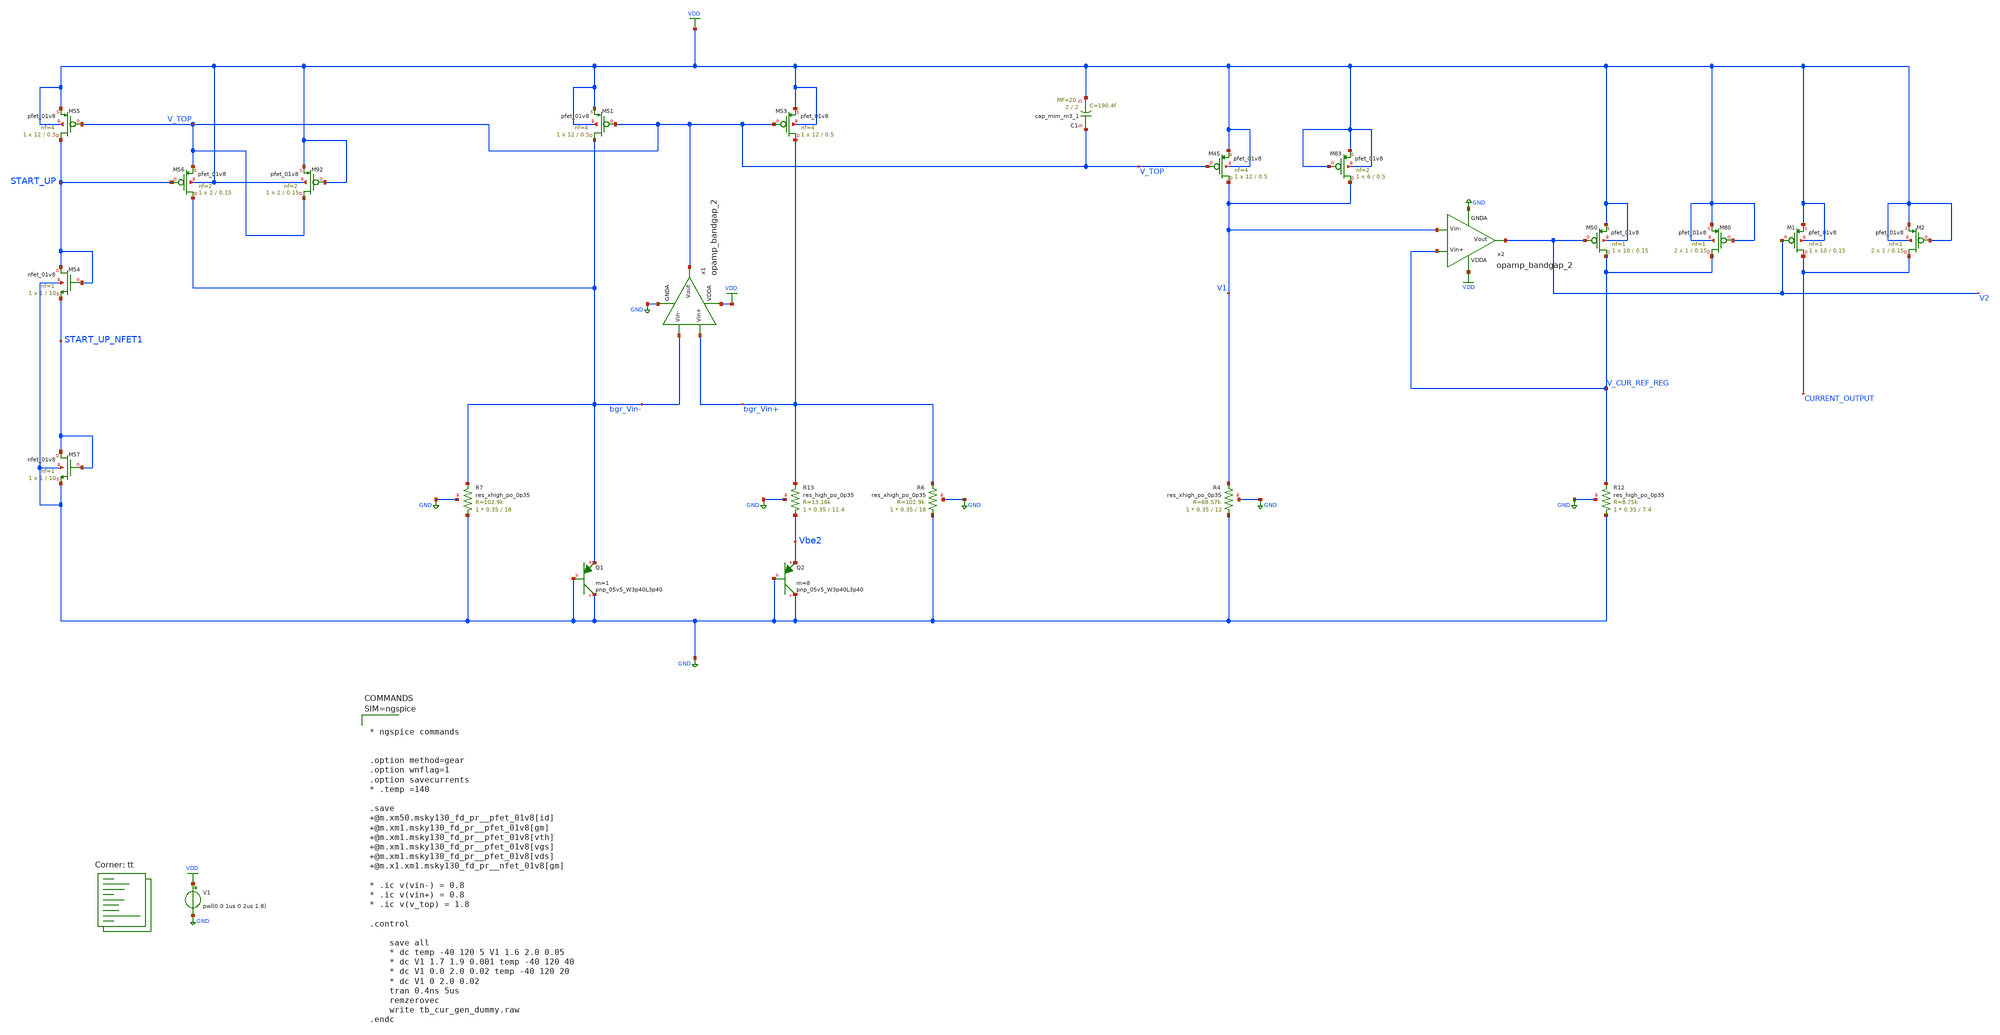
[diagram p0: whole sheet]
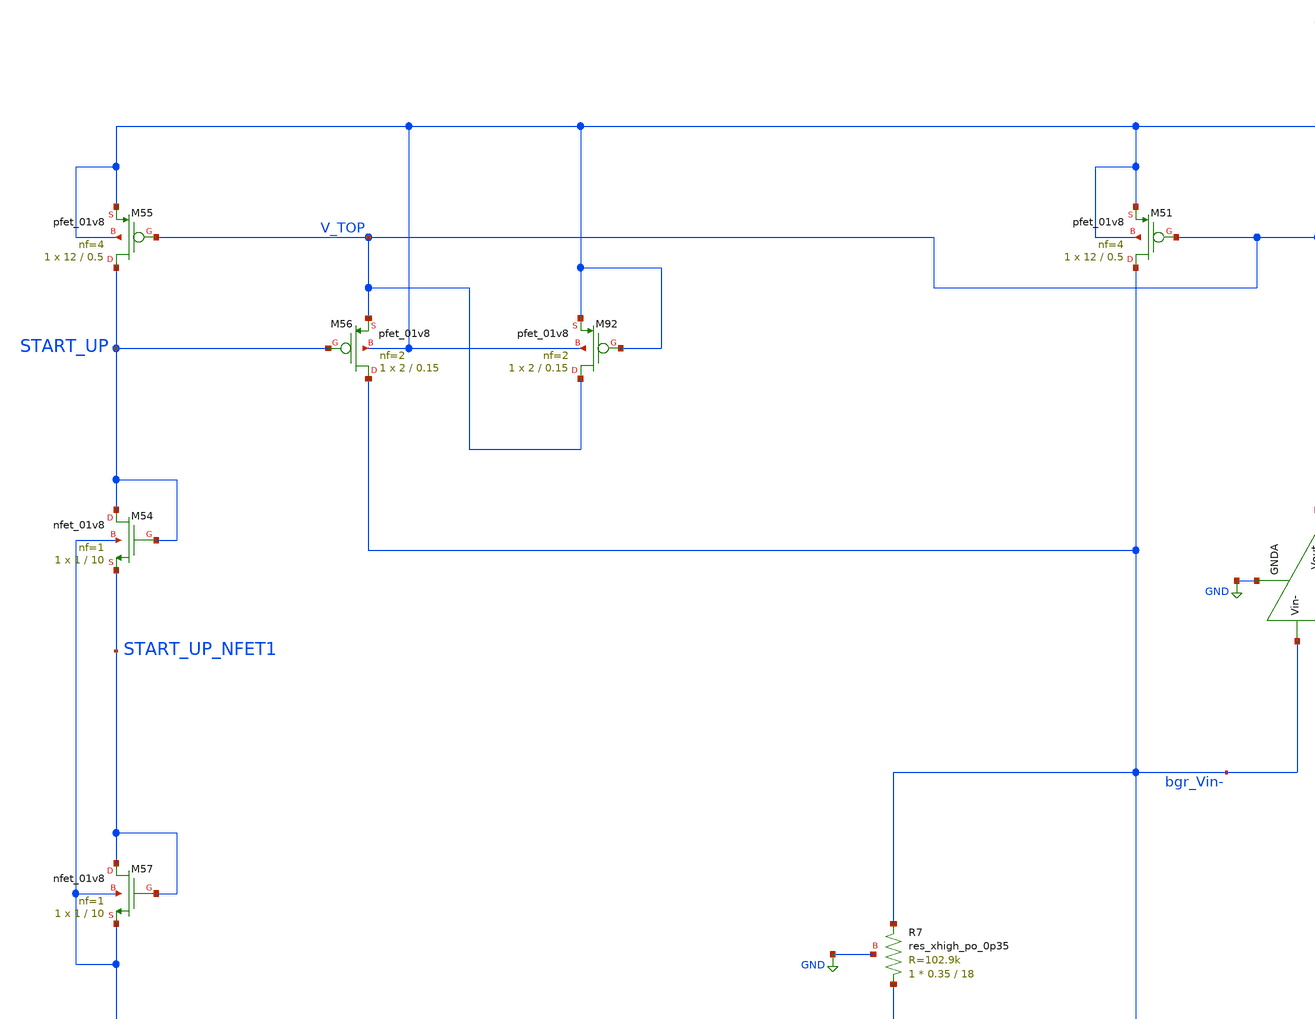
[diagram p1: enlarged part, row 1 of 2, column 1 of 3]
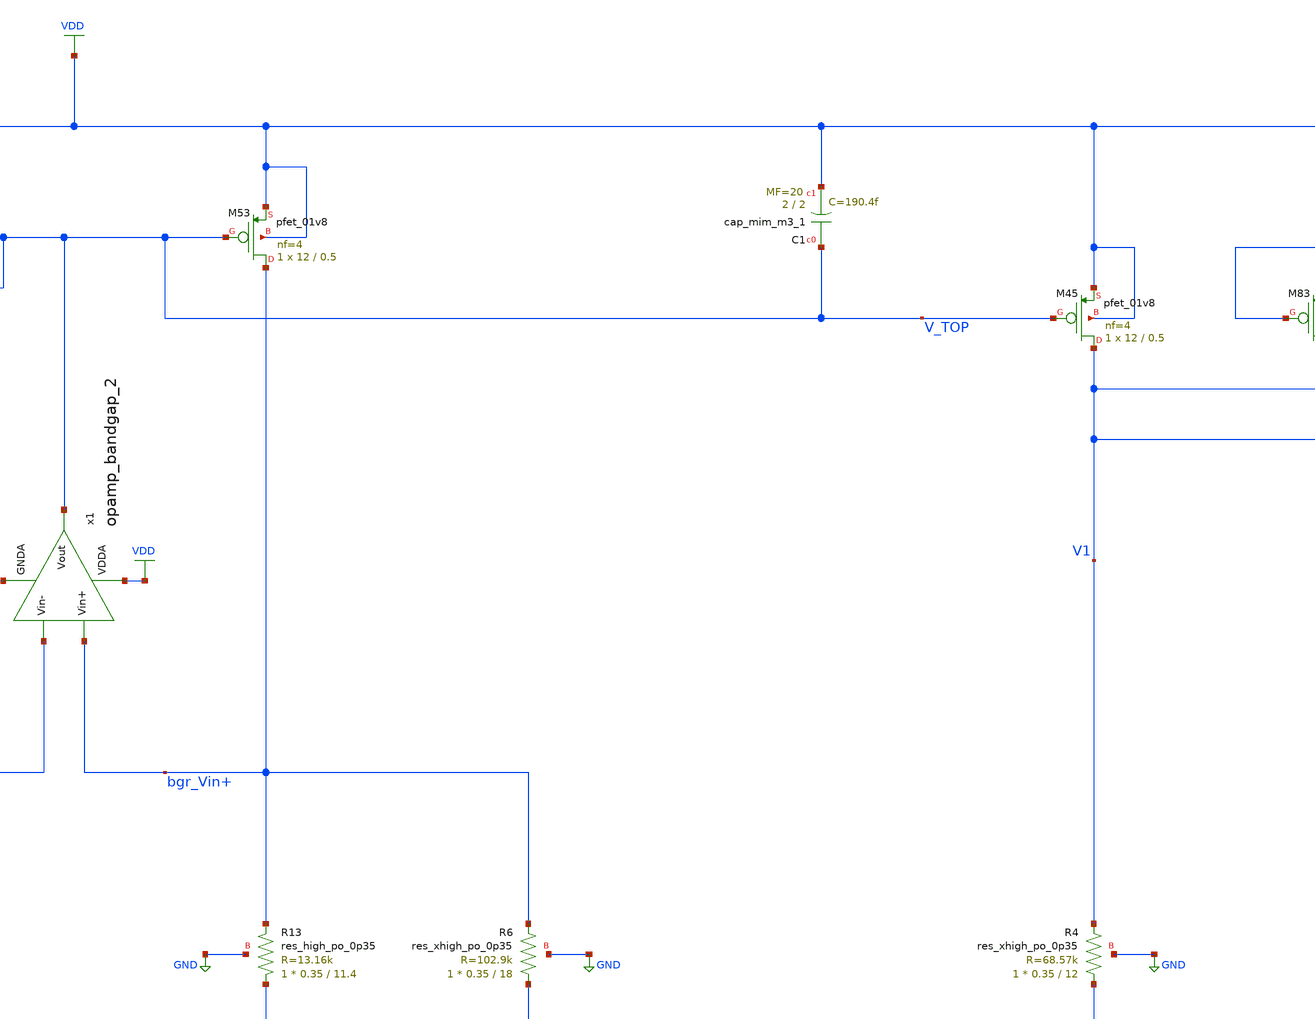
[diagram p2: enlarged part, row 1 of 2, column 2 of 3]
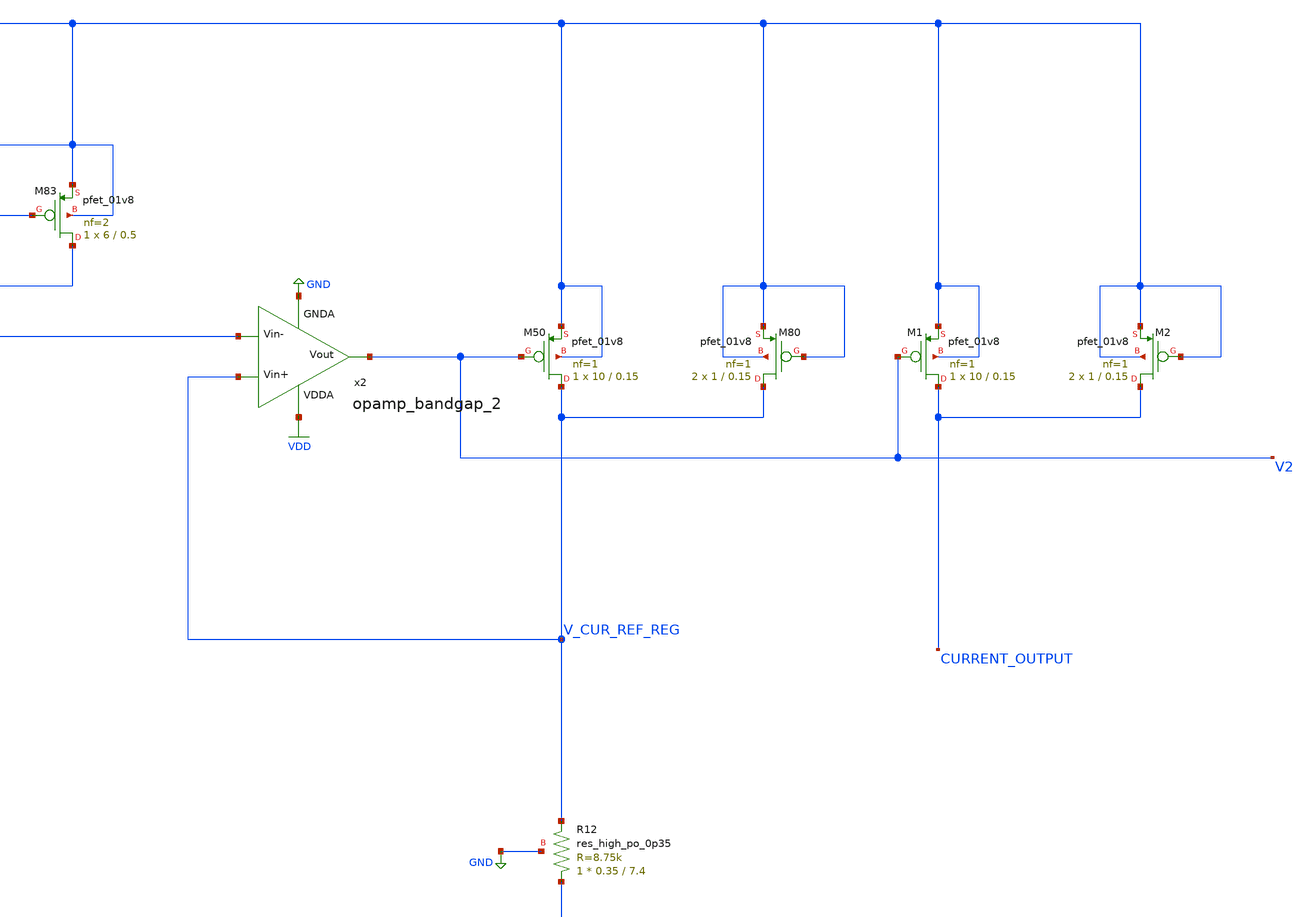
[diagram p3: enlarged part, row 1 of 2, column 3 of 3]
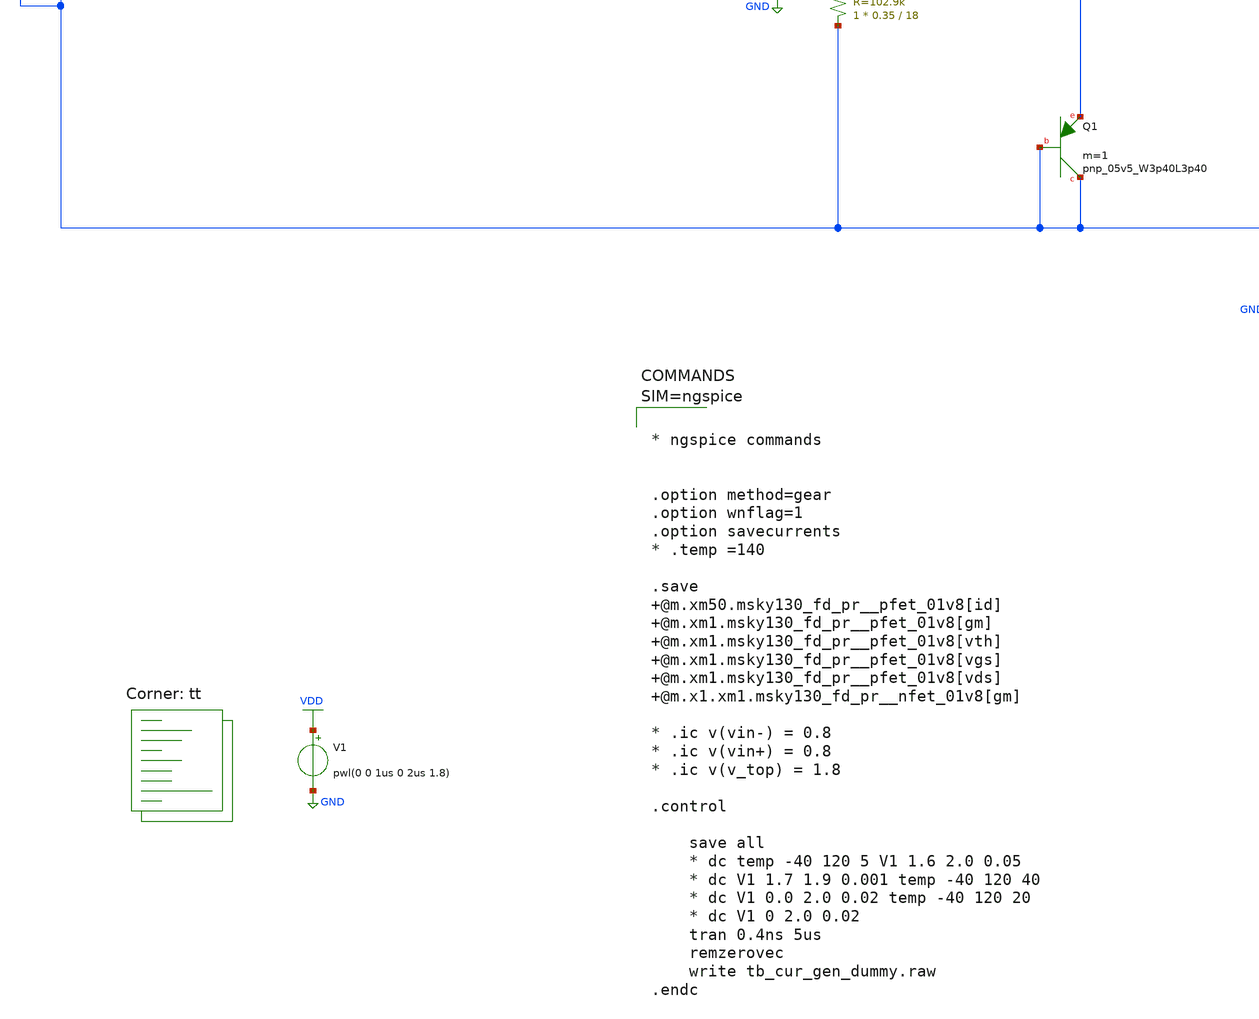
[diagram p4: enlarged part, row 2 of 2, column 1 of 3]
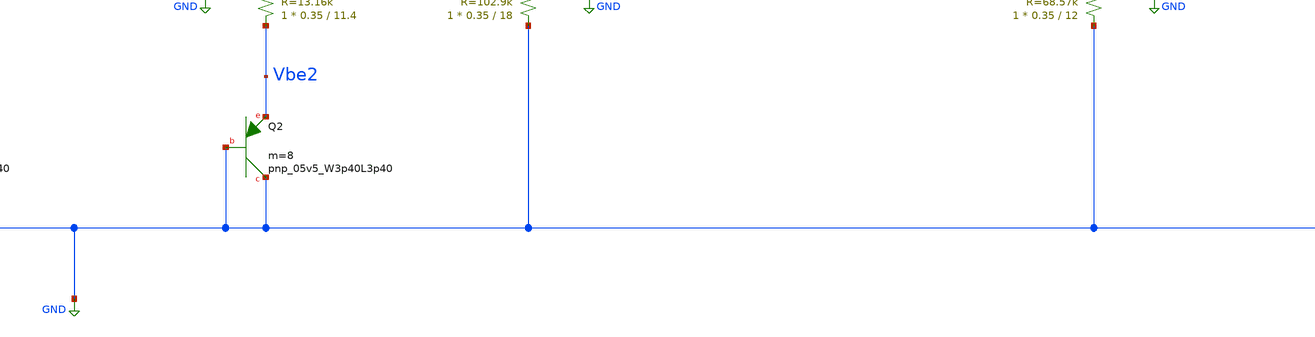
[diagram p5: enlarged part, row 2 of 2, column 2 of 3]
** sch_path: projects/pll/full_pll/xschem_ngspice/tb_cur_gen_dummy.sch
**.subckt tb_cur_gen_dummy
V1 VDD GND pwl(0 0 1us 0 2us 1.8)
XM45 V1 V_TOP VDD VDD sky130_fd_pr__pfet_01v8 L=0.5 W=12 nf=4 ad='int((nf+1)/2) * W/nf * 0.29' as='int((nf+2)/2) * W/nf * 0.29'
+ pd='2*int((nf+1)/2) * (W/nf + 0.29)' ps='2*int((nf+2)/2) * (W/nf + 0.29)' nrd='0.29 / W' nrs='0.29 / W'
+ sa=0 sb=0 sd=0 mult=1 m=1
XR4 GND V1 GND sky130_fd_pr__res_xhigh_po_0p35 L=12 mult=1 m=1
XM50 V_CUR_REF_REG V2 VDD VDD sky130_fd_pr__pfet_01v8 L=0.15 W=10 nf=1 ad='int((nf+1)/2) * W/nf * 0.29'
+ as='int((nf+2)/2) * W/nf * 0.29' pd='2*int((nf+1)/2) * (W/nf + 0.29)' ps='2*int((nf+2)/2) * (W/nf + 0.29)'
+ nrd='0.29 / W' nrs='0.29 / W' sa=0 sb=0 sd=0 mult=1 m=1
XC1 V_TOP VDD sky130_fd_pr__cap_mim_m3_1 W=2 L=2 MF=20 m=20
XQ1 GND GND bgr_Vin- sky130_fd_pr__pnp_05v5_W3p40L3p40 m=1
XQ2 GND GND Vbe2 sky130_fd_pr__pnp_05v5_W3p40L3p40 m=8
XM51 bgr_Vin- V_TOP VDD VDD sky130_fd_pr__pfet_01v8 L=0.5 W=12 nf=4 ad='int((nf+1)/2) * W/nf * 0.29'
+ as='int((nf+2)/2) * W/nf * 0.29' pd='2*int((nf+1)/2) * (W/nf + 0.29)' ps='2*int((nf+2)/2) * (W/nf + 0.29)'
+ nrd='0.29 / W' nrs='0.29 / W' sa=0 sb=0 sd=0 mult=1 m=1
XM53 bgr_Vin+ V_TOP VDD VDD sky130_fd_pr__pfet_01v8 L=0.5 W=12 nf=4 ad='int((nf+1)/2) * W/nf * 0.29'
+ as='int((nf+2)/2) * W/nf * 0.29' pd='2*int((nf+1)/2) * (W/nf + 0.29)' ps='2*int((nf+2)/2) * (W/nf + 0.29)'
+ nrd='0.29 / W' nrs='0.29 / W' sa=0 sb=0 sd=0 mult=1 m=1
XR6 GND bgr_Vin+ GND sky130_fd_pr__res_xhigh_po_0p35 L=18 mult=1 m=1
XR7 GND bgr_Vin- GND sky130_fd_pr__res_xhigh_po_0p35 L=18 mult=1 m=1
XM54 START_UP START_UP START_UP_NFET1 GND sky130_fd_pr__nfet_01v8 L=10 W=1 nf=1 ad='int((nf+1)/2) * W/nf * 0.29'
+ as='int((nf+2)/2) * W/nf * 0.29' pd='2*int((nf+1)/2) * (W/nf + 0.29)' ps='2*int((nf+2)/2) * (W/nf + 0.29)'
+ nrd='0.29 / W' nrs='0.29 / W' sa=0 sb=0 sd=0 mult=1 m=1
XM55 START_UP V_TOP VDD VDD sky130_fd_pr__pfet_01v8 L=0.5 W=12 nf=4 ad='int((nf+1)/2) * W/nf * 0.29'
+ as='int((nf+2)/2) * W/nf * 0.29' pd='2*int((nf+1)/2) * (W/nf + 0.29)' ps='2*int((nf+2)/2) * (W/nf + 0.29)'
+ nrd='0.29 / W' nrs='0.29 / W' sa=0 sb=0 sd=0 mult=1 m=1
XM56 bgr_Vin- START_UP V_TOP VDD sky130_fd_pr__pfet_01v8 L=0.15 W=2 nf=2 ad='int((nf+1)/2) * W/nf * 0.29'
+ as='int((nf+2)/2) * W/nf * 0.29' pd='2*int((nf+1)/2) * (W/nf + 0.29)' ps='2*int((nf+2)/2) * (W/nf + 0.29)'
+ nrd='0.29 / W' nrs='0.29 / W' sa=0 sb=0 sd=0 mult=1 m=1
XM57 START_UP_NFET1 START_UP_NFET1 GND GND sky130_fd_pr__nfet_01v8 L=10 W=1 nf=1 ad='int((nf+1)/2) * W/nf * 0.29'
+ as='int((nf+2)/2) * W/nf * 0.29' pd='2*int((nf+1)/2) * (W/nf + 0.29)' ps='2*int((nf+2)/2) * (W/nf + 0.29)'
+ nrd='0.29 / W' nrs='0.29 / W' sa=0 sb=0 sd=0 mult=1 m=1
x1 VDD V_TOP bgr_Vin- bgr_Vin+ GND opamp_bandgap_2
x2 VDD V2 V1 V_CUR_REF_REG GND opamp_bandgap_2
XM80 V_CUR_REF_REG VDD VDD VDD sky130_fd_pr__pfet_01v8 L=0.15 W=1 nf=1 ad='int((nf+1)/2) * W/nf * 0.29'
+ as='int((nf+2)/2) * W/nf * 0.29' pd='2*int((nf+1)/2) * (W/nf + 0.29)' ps='2*int((nf+2)/2) * (W/nf + 0.29)'
+ nrd='0.29 / W' nrs='0.29 / W' sa=0 sb=0 sd=0 mult=2 m=2
XM83 V1 VDD VDD VDD sky130_fd_pr__pfet_01v8 L=0.5 W=6 nf=2 ad='int((nf+1)/2) * W/nf * 0.29' as='int((nf+2)/2) * W/nf * 0.29'
+ pd='2*int((nf+1)/2) * (W/nf + 0.29)' ps='2*int((nf+2)/2) * (W/nf + 0.29)' nrd='0.29 / W' nrs='0.29 / W'
+ sa=0 sb=0 sd=0 mult=1 m=1
XM92 V_TOP VDD VDD VDD sky130_fd_pr__pfet_01v8 L=0.15 W=2 nf=2 ad='int((nf+1)/2) * W/nf * 0.29' as='int((nf+2)/2) * W/nf * 0.29'
+ pd='2*int((nf+1)/2) * (W/nf + 0.29)' ps='2*int((nf+2)/2) * (W/nf + 0.29)' nrd='0.29 / W' nrs='0.29 / W'
+ sa=0 sb=0 sd=0 mult=1 m=1
XM1 CURRENT_OUTPUT V2 VDD VDD sky130_fd_pr__pfet_01v8 L=0.15 W=10 nf=1 ad='int((nf+1)/2) * W/nf * 0.29'
+ as='int((nf+2)/2) * W/nf * 0.29' pd='2*int((nf+1)/2) * (W/nf + 0.29)' ps='2*int((nf+2)/2) * (W/nf + 0.29)'
+ nrd='0.29 / W' nrs='0.29 / W' sa=0 sb=0 sd=0 mult=1 m=1
XM2 CURRENT_OUTPUT VDD VDD VDD sky130_fd_pr__pfet_01v8 L=0.15 W=1 nf=1 ad='int((nf+1)/2) * W/nf * 0.29'
+ as='int((nf+2)/2) * W/nf * 0.29' pd='2*int((nf+1)/2) * (W/nf + 0.29)' ps='2*int((nf+2)/2) * (W/nf + 0.29)'
+ nrd='0.29 / W' nrs='0.29 / W' sa=0 sb=0 sd=0 mult=2 m=2
XR12 GND V_CUR_REF_REG GND sky130_fd_pr__res_high_po_0p35 L=7.4 mult=1 m=1
XR13 Vbe2 bgr_Vin+ GND sky130_fd_pr__res_high_po_0p35 L=11.4 mult=1 m=1
**** begin user architecture code
.lib $::SKYWATER_MODELS/sky130.lib.spice tt



* ngspice commands


.option method=gear
.option wnflag=1
.option savecurrents
* .temp =140

.save @m.xm50.msky130_fd_pr__pfet_01v8[id] @m.xm1.msky130_fd_pr__pfet_01v8[gm] @m.xm1.msky130_fd_pr__pfet_01v8[vth] @m.xm1.msky130_fd_pr__pfet_01v8[vgs] @m.xm1.msky130_fd_pr__pfet_01v8[vds] @m.x1.xm1.msky130_fd_pr__nfet_01v8[gm]

* .ic v(vin-) = 0.8
* .ic v(vin+) = 0.8
* .ic v(v_top) = 1.8

.control

    save all
    * dc temp -40 120 5 V1 1.6 2.0 0.05
    * dc V1 1.7 1.9 0.001 temp -40 120 40
    * dc V1 0.0 2.0 0.02 temp -40 120 20
    * dc V1 0 2.0 0.02
    tran 0.4ns 5us
    remzerovec
    write tb_cur_gen_dummy.raw
.endc




**** end user architecture code
**.ends

* expanding   symbol:
*+  /foss/designs/my_design/projects/bandgapref/xschem_ngspice/new_files/opamp_bandgap_2.sym # of pins=5
** sym_path: projects/bandgapref/xschem_ngspice/new_files/opamp_bandgap_2.sym
** sch_path: projects/bandgapref/xschem_ngspice/new_files/opamp_bandgap_2.sch
.subckt opamp_bandgap_2 VDDA Vout Vin- Vin+ GNDA
*.ipin Vin+
*.opin Vout
*.ipin Vin-
*.ipin GNDA
*.ipin VDDA
XM1 V_p VDDA GNDA GNDA sky130_fd_pr__nfet_01v8 L=5 W=2.5 nf=1 ad='int((nf+1)/2) * W/nf * 0.29' as='int((nf+2)/2) * W/nf * 0.29'
+ pd='2*int((nf+1)/2) * (W/nf + 0.29)' ps='2*int((nf+2)/2) * (W/nf + 0.29)' nrd='0.29 / W' nrs='0.29 / W'
+ sa=0 sb=0 sd=0 mult=1 m=1
XM2 V_mirror Vin- V_p GNDA sky130_fd_pr__nfet_01v8 L=0.2 W=2.5 nf=1 ad='int((nf+1)/2) * W/nf * 0.29'
+ as='int((nf+2)/2) * W/nf * 0.29' pd='2*int((nf+1)/2) * (W/nf + 0.29)' ps='2*int((nf+2)/2) * (W/nf + 0.29)'
+ nrd='0.29 / W' nrs='0.29 / W' sa=0 sb=0 sd=0 mult=1 m=1
XM3 1st_Vout Vin+ V_p GNDA sky130_fd_pr__nfet_01v8 L=0.2 W=2.5 nf=1 ad='int((nf+1)/2) * W/nf * 0.29'
+ as='int((nf+2)/2) * W/nf * 0.29' pd='2*int((nf+1)/2) * (W/nf + 0.29)' ps='2*int((nf+2)/2) * (W/nf + 0.29)'
+ nrd='0.29 / W' nrs='0.29 / W' sa=0 sb=0 sd=0 mult=1 m=1
XM5 V_mirror V_mirror VDDA VDDA sky130_fd_pr__pfet_01v8 L=0.2 W=6 nf=2 ad='int((nf+1)/2) * W/nf * 0.29'
+ as='int((nf+2)/2) * W/nf * 0.29' pd='2*int((nf+1)/2) * (W/nf + 0.29)' ps='2*int((nf+2)/2) * (W/nf + 0.29)'
+ nrd='0.29 / W' nrs='0.29 / W' sa=0 sb=0 sd=0 mult=1 m=1
XM6 1st_Vout V_mirror VDDA VDDA sky130_fd_pr__pfet_01v8 L=0.2 W=6 nf=2 ad='int((nf+1)/2) * W/nf * 0.29'
+ as='int((nf+2)/2) * W/nf * 0.29' pd='2*int((nf+1)/2) * (W/nf + 0.29)' ps='2*int((nf+2)/2) * (W/nf + 0.29)'
+ nrd='0.29 / W' nrs='0.29 / W' sa=0 sb=0 sd=0 mult=1 m=1
XM4 Vout VDDA GNDA GNDA sky130_fd_pr__nfet_01v8 L=5 W=2.5 nf=1 ad='int((nf+1)/2) * W/nf * 0.29' as='int((nf+2)/2) * W/nf * 0.29'
+ pd='2*int((nf+1)/2) * (W/nf + 0.29)' ps='2*int((nf+2)/2) * (W/nf + 0.29)' nrd='0.29 / W' nrs='0.29 / W'
+ sa=0 sb=0 sd=0 mult=1 m=1
XM7 Vout 1st_Vout VDDA VDDA sky130_fd_pr__pfet_01v8 L=0.2 W=6 nf=2 ad='int((nf+1)/2) * W/nf * 0.29' as='int((nf+2)/2) * W/nf * 0.29'
+ pd='2*int((nf+1)/2) * (W/nf + 0.29)' ps='2*int((nf+2)/2) * (W/nf + 0.29)' nrd='0.29 / W' nrs='0.29 / W'
+ sa=0 sb=0 sd=0 mult=1 m=1
XC1 1st_Vout cap_res sky130_fd_pr__cap_mim_m3_1 W=2 L=2 MF=20 m=20
XM8 Vout VDDA VDDA VDDA sky130_fd_pr__pfet_01v8 L=0.2 W=1 nf=1 ad='int((nf+1)/2) * W/nf * 0.29' as='int((nf+2)/2) * W/nf * 0.29'
+ pd='2*int((nf+1)/2) * (W/nf + 0.29)' ps='2*int((nf+2)/2) * (W/nf + 0.29)' nrd='0.29 / W' nrs='0.29 / W'
+ sa=0 sb=0 sd=0 mult=2 m=2
XR1 Vout cap_res GNDA sky130_fd_pr__res_high_po_0p69 L=5 mult=1 m=1
.ends

.GLOBAL GND
.GLOBAL VDD
.end
